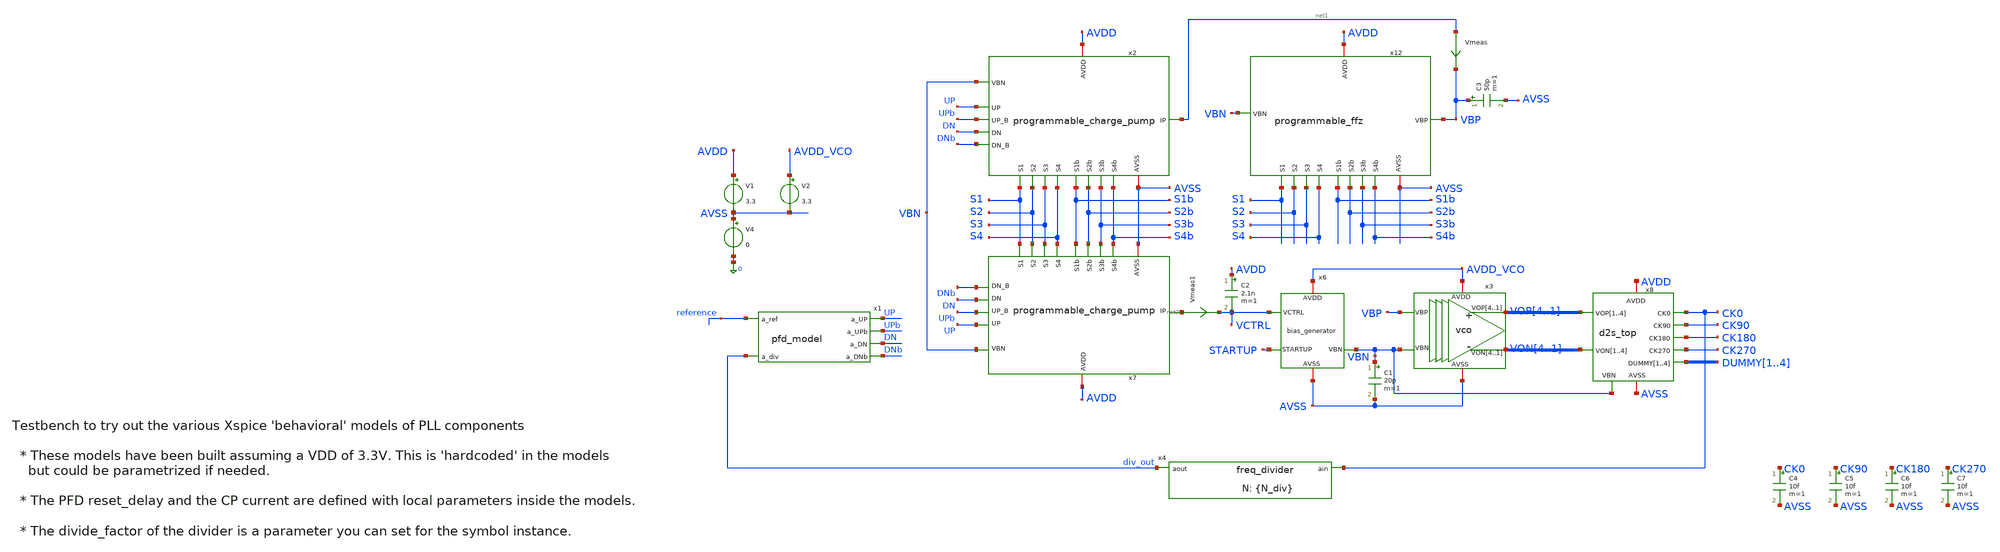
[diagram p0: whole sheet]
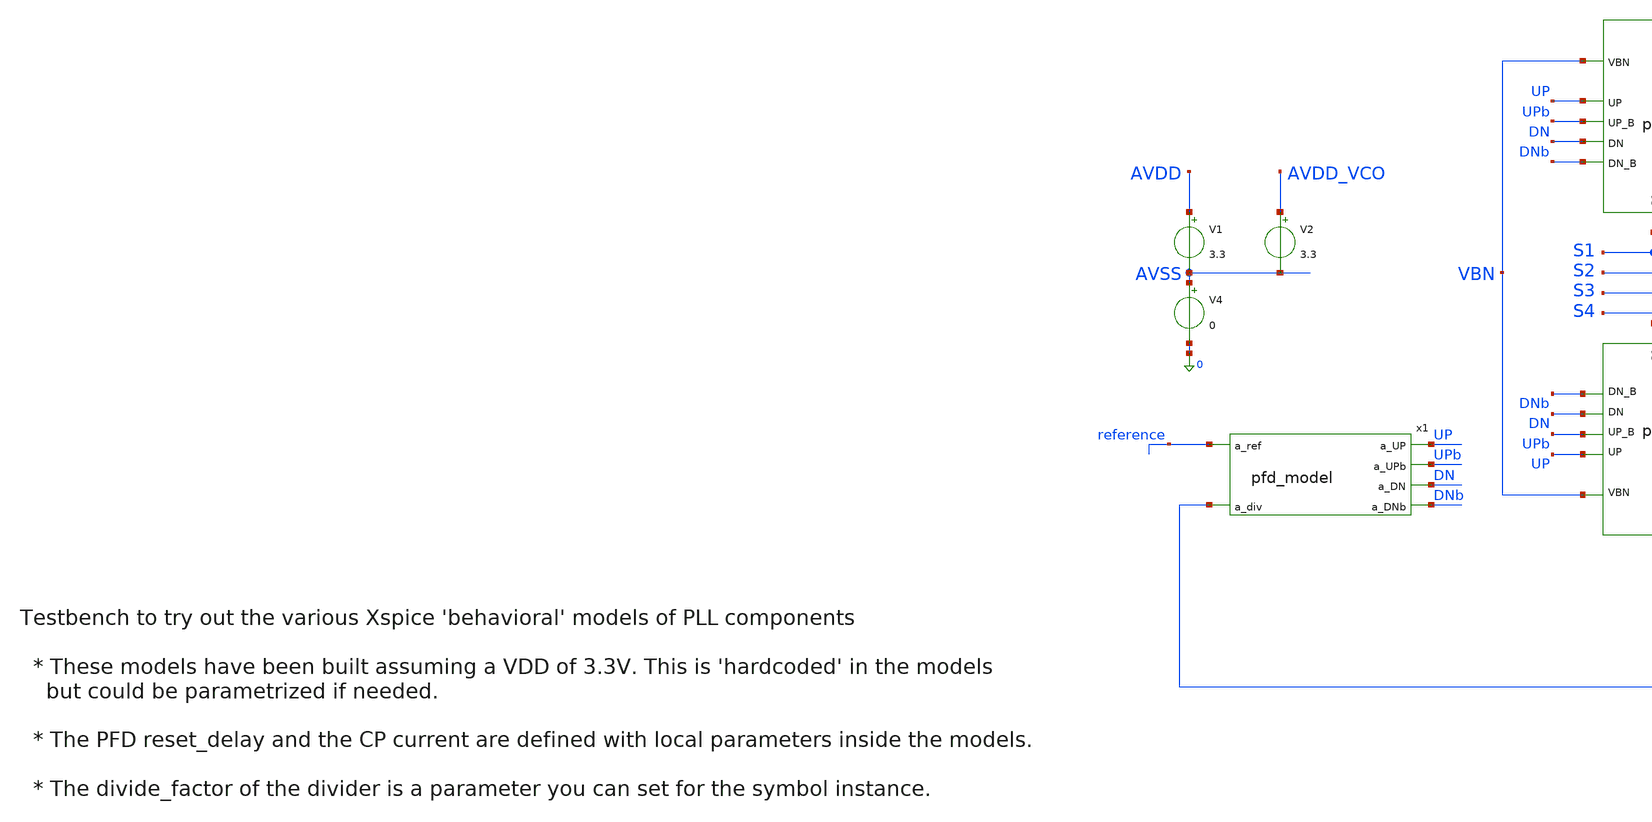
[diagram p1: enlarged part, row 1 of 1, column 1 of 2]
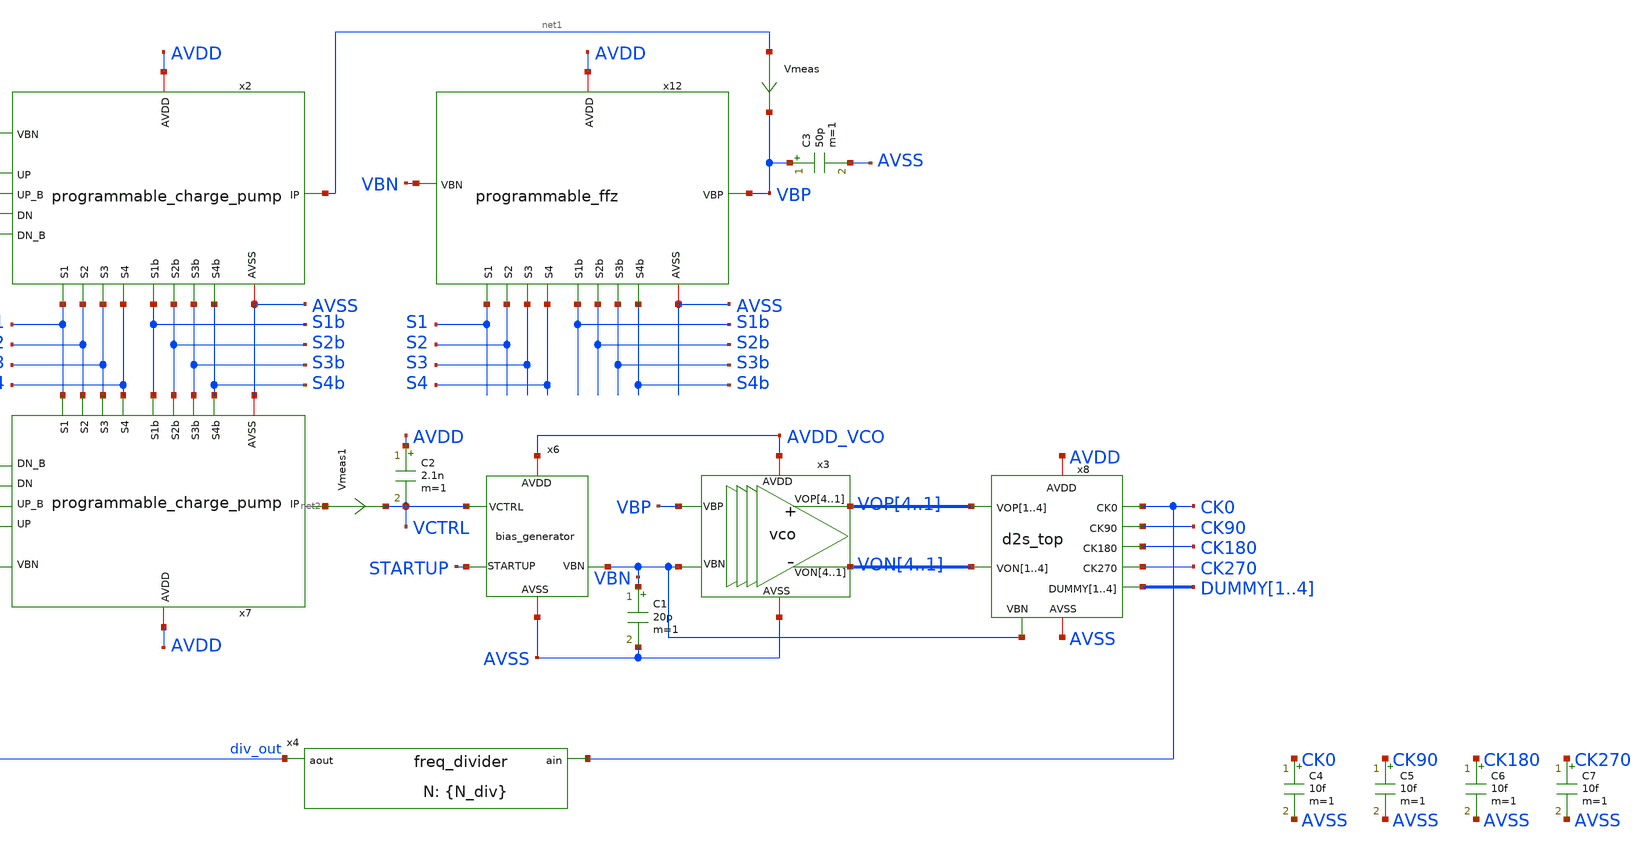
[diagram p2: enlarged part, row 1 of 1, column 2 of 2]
** sch_path: designs/libs/tb_pll/tb_PLL_CP_VCO_model_v2.sch
**.subckt tb_PLL_CP_VCO_model_v2
x1 reference UP UPb DN div_out DNb pfd_model
x4 div_out CK0 freq_divider divide_factor={N_div}
x3 VOP4 VOP3 VOP2 VOP1 VON4 VON3 VON2 VON1 AVDD_VCO AVSS VBP VBN vco
x6 VCTRL AVDD_VCO STARTUP AVSS VBN bias_generator
C2 AVDD VCTRL 2.1n m=1
V1 AVDD AVSS 3.3
V4 AVSS 0 0
V2 AVDD_VCO AVSS 3.3
x2 AVSS AVDD UP UPb DN net1 DNb VBN S1b S1 S2b S2 S3b S3 S4b S4 programmable_charge_pump
x7 AVSS AVDD UP UPb DN net2 DNb VBN S1b S1 S2b S2 S3b S3 S4b S4 programmable_charge_pump
Vmeas net1 VBP 0
.save i(vmeas)
Vmeas1 net2 VCTRL 0
.save i(vmeas1)
C1 VBN AVSS 20p m=1
C3 VBP AVSS 50p m=1
x12 VBP AVSS AVDD VBN S1b S1 S2b S2 S3b S3 S4b S4 programmable_ffz
x8 VOP4 VOP3 VOP2 VOP1 VON4 VON3 VON2 VON1 VBN DUMMY1 DUMMY2 DUMMY3 DUMMY4 CK0 CK90 CK180 CK270 AVDD
+ AVSS d2s_top
C4 CK0 AVSS 10f m=1
C5 CK90 AVSS 10f m=1
C6 CK180 AVSS 10f m=1
C7 CK270 AVSS 10f m=1
**** begin user architecture code


.param f_ref=10k R_div=2 N_div=2
*.param f_ref=2e3 R_div=2 N_div=255
.param tp_ref='td_ref/2' td_ref='1/f_ref'
Vref reference gnd pulse(0 3.3 0 10p 10p tp_ref td_ref)

.ic v(VCTRL)=2.6 v(vbp)=2.6
*.ic v(VCTRL)=1 v(vbp)=1

.ic v(vop1)=3.3 v(von1)=0 v(startup)=0
.options reltol=1e-5 cshunt=1e-15
.options method=gear

*.param d1=0 d2=0 d3=0 d4=0
*.param d1b=3.3 d2b=3.3 d3b=3.3 d4b=3.3

.param d1=3.3 d2=3.3 d3=3.3 d4=3.3
.param d1b=0 d2b=0 d3b=0 d4b=0

VS1 S1 0 d1
VS2 S2 0 d2
VS3 S3 0 d3
VS4 S4 0 d4

VS1b S1b 0 d1b
VS2b S2b 0 d2b
VS3b S3b 0 d3b
VS4b S4b 0 d4b

.control
set wr_singlescale
set wr_vecnames

* save all
*save v(VCTRL) v(vbp) v(vbn)
*+v(reference) v(div_out) v(pre_div)
*+v(CK0) v(CK90) v(CK180) v(CK270) v(up) v(dn)

*v(vop1) v(von1) v(vop3) v(von3)

*OP
*show all

*tran 100n 20m
*tran 0.1n 20u



*write tb1.raw
*wrdata /foss/designs/synchronos-chipathon-2026/designs/libs/scripts/sim_data/tb1.txt tran.all
save v(CK0)
tran 100n 20m 5m
linearize v(CK0)
fft v(CK0)
write tb1_fft.raw
  *wrdata tl_synth_tb_long_2.txt v(vfout)
.endc



.include $::180MCU_MODELS/design.ngspice
.lib $::180MCU_MODELS/sm141064.ngspice typical
*.lib $::180MCU_MODELS/sm141064.ngspice SS
*.lib $::180MCU_MODELS/sm141064.ngspice FF
*.lib $::180MCU_MODELS/sm141064.ngspice SF
*.lib $::180MCU_MODELS/sm141064.ngspice FS

**** end user architecture code
**.ends
.end
